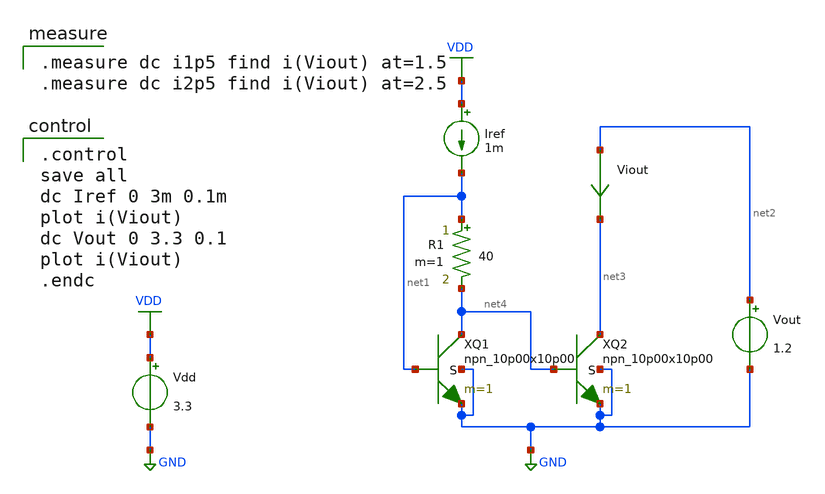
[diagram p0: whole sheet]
** sch_path: current-source/cm-nagata-bjt.sch
**.subckt cm-nagata-bjt
XQ2 net3 net4 GND GND npn_10p00x10p00 m=1
XQ1 net4 net1 GND GND npn_10p00x10p00 m=1
Viout net2 net3 0
.save i(viout)
Vdd VDD GND 3.3
Iref VDD net1 1m
Vout net2 GND 1.2
R1 net1 net4 40 m=1
**** begin user architecture code

.include $::180MCU_MODELS/design.ngspice
.lib $::180MCU_MODELS/sm141064.ngspice typical
.lib $::180MCU_MODELS/sm141064.ngspice res_typical
.lib $::180MCU_MODELS/sm141064.ngspice moscap_typical
.lib $::180MCU_MODELS/sm141064.ngspice bjt_typical
* .lib $::180MCU_MODELS/sm141064.ngspice res_statistical


.control
save all
dc Iref 0 3m 0.1m
plot i(Viout)
dc Vout 0 3.3 0.1
plot i(Viout)
.endc


.measure dc i1p5 find i(Viout) at=1.5
.measure dc i2p5 find i(Viout) at=2.5

**** end user architecture code
**.ends
.GLOBAL GND
.GLOBAL VDD
.end
